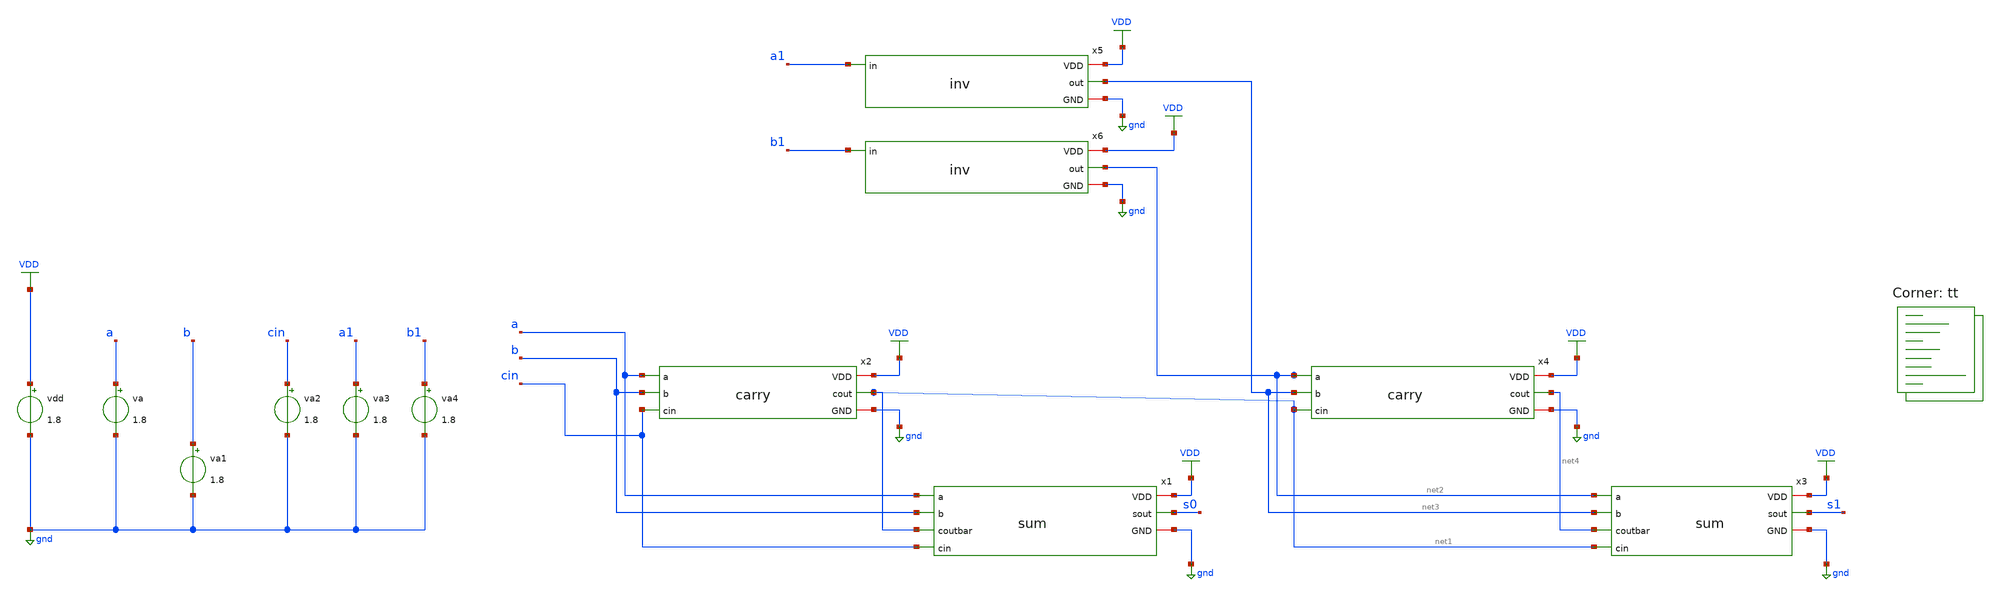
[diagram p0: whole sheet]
** sch_path: assignments/assignment7/assign1a.sch
**.subckt assign1a
x1 VDD a b net1 cin s0 gnd sum
x2 VDD a b cin net1 gnd carry
x3 VDD net2 net3 net4 net1 s1 gnd sum
x4 VDD net2 net3 net1 net4 gnd carry
vdd VDD gnd 1.8
va a gnd 1.8
va1 b gnd 1.8
va2 cin gnd 1.8
va3 a1 gnd 1.8
va4 b1 gnd 1.8
x5 VDD a1 net3 gnd inv
x6 VDD b1 net2 gnd inv
**** begin user architecture code


.control
alter @va[pulse] = [ 1.8 0 10p 5p 5p ]
alter @va1[pulse] = [ 1.8 0 10p 5p 5p ]
alter @va2[pulse] = [ 0 1.8 10p 5p 5p ]
alter @va3[pulse] = [ 1.8 0 10p 5p 5p ]
alter @va4[pulse] = [ 1.8 0 10p 5p 5p ]

tran 1p 400p
meas tran delay_cin_net1 TRIG v(cin) VAL=0.9 RISE=1 TARG v(net1) VAL=0.9 FALL=1
meas tran delay_cin_s0 TRIG v(cin) VAL=0.9 RISE=1 TARG v(s0) VAL=0.9 CROSS=1
plot v(a) v(b) v(cin) v(s0)
.endc


.lib $::SKYWATER_MODELS/sky130.lib.spice tt
**** end user architecture code
**.ends

* expanding   symbol:  sum.sym # of pins=7
** sym_path: assignments/assignment7/sum.sym
** sch_path: assignments/assignment7/sum.sch
.subckt sum VDD a b coutbar cin sout GND
*.opin sout
*.ipin a
*.iopin VDD
*.iopin GND
*.ipin b
*.ipin coutbar
*.ipin cin
XM1 sout coutbar net4 GND sky130_fd_pr__nfet_01v8 L=0.15 W=0.84 nf=1 ad='int((nf+1)/2) * W/nf * 0.29'
+ as='int((nf+2)/2) * W/nf * 0.29' pd='2*int((nf+1)/2) * (W/nf + 0.29)' ps='2*int((nf+2)/2) * (W/nf + 0.29)'
+ nrd='0.29 / W' nrs='0.29 / W' sa=0 sb=0 sd=0 mult=1 m=1
XM2 net1 b VDD VDD sky130_fd_pr__pfet_01v8 L=0.15 W=1.68 nf=1 ad='int((nf+1)/2) * W/nf * 0.29' as='int((nf+2)/2) * W/nf * 0.29'
+ pd='2*int((nf+1)/2) * (W/nf + 0.29)' ps='2*int((nf+2)/2) * (W/nf + 0.29)' nrd='0.29 / W' nrs='0.29 / W'
+ sa=0 sb=0 sd=0 mult=1 m=1
XM4 sout coutbar net1 VDD sky130_fd_pr__pfet_01v8 L=0.15 W=1.68 nf=1 ad='int((nf+1)/2) * W/nf * 0.29'
+ as='int((nf+2)/2) * W/nf * 0.29' pd='2*int((nf+1)/2) * (W/nf + 0.29)' ps='2*int((nf+2)/2) * (W/nf + 0.29)'
+ nrd='0.29 / W' nrs='0.29 / W' sa=0 sb=0 sd=0 mult=1 m=1
XM5 net1 a VDD VDD sky130_fd_pr__pfet_01v8 L=0.15 W=1.68 nf=1 ad='int((nf+1)/2) * W/nf * 0.29' as='int((nf+2)/2) * W/nf * 0.29'
+ pd='2*int((nf+1)/2) * (W/nf + 0.29)' ps='2*int((nf+2)/2) * (W/nf + 0.29)' nrd='0.29 / W' nrs='0.29 / W'
+ sa=0 sb=0 sd=0 mult=1 m=1
XM6 net1 cin VDD VDD sky130_fd_pr__pfet_01v8 L=0.15 W=1.68 nf=1 ad='int((nf+1)/2) * W/nf * 0.29' as='int((nf+2)/2) * W/nf * 0.29'
+ pd='2*int((nf+1)/2) * (W/nf + 0.29)' ps='2*int((nf+2)/2) * (W/nf + 0.29)' nrd='0.29 / W' nrs='0.29 / W'
+ sa=0 sb=0 sd=0 mult=1 m=1
XM7 net3 a VDD VDD sky130_fd_pr__pfet_01v8 L=0.15 W=1.68 nf=1 ad='int((nf+1)/2) * W/nf * 0.29' as='int((nf+2)/2) * W/nf * 0.29'
+ pd='2*int((nf+1)/2) * (W/nf + 0.29)' ps='2*int((nf+2)/2) * (W/nf + 0.29)' nrd='0.29 / W' nrs='0.29 / W'
+ sa=0 sb=0 sd=0 mult=1 m=1
XM3 net2 b net3 VDD sky130_fd_pr__pfet_01v8 L=0.15 W=1.68 nf=1 ad='int((nf+1)/2) * W/nf * 0.29' as='int((nf+2)/2) * W/nf * 0.29'
+ pd='2*int((nf+1)/2) * (W/nf + 0.29)' ps='2*int((nf+2)/2) * (W/nf + 0.29)' nrd='0.29 / W' nrs='0.29 / W'
+ sa=0 sb=0 sd=0 mult=1 m=1
XM8 sout cin net2 VDD sky130_fd_pr__pfet_01v8 L=0.15 W=1.68 nf=1 ad='int((nf+1)/2) * W/nf * 0.29' as='int((nf+2)/2) * W/nf * 0.29'
+ pd='2*int((nf+1)/2) * (W/nf + 0.29)' ps='2*int((nf+2)/2) * (W/nf + 0.29)' nrd='0.29 / W' nrs='0.29 / W'
+ sa=0 sb=0 sd=0 mult=1 m=1
XM9 net4 a GND GND sky130_fd_pr__nfet_01v8 L=0.15 W=0.84 nf=1 ad='int((nf+1)/2) * W/nf * 0.29' as='int((nf+2)/2) * W/nf * 0.29'
+ pd='2*int((nf+1)/2) * (W/nf + 0.29)' ps='2*int((nf+2)/2) * (W/nf + 0.29)' nrd='0.29 / W' nrs='0.29 / W'
+ sa=0 sb=0 sd=0 mult=1 m=1
XM10 net4 b GND GND sky130_fd_pr__nfet_01v8 L=0.15 W=0.84 nf=1 ad='int((nf+1)/2) * W/nf * 0.29' as='int((nf+2)/2) * W/nf * 0.29'
+ pd='2*int((nf+1)/2) * (W/nf + 0.29)' ps='2*int((nf+2)/2) * (W/nf + 0.29)' nrd='0.29 / W' nrs='0.29 / W'
+ sa=0 sb=0 sd=0 mult=1 m=1
XM11 net4 cin GND GND sky130_fd_pr__nfet_01v8 L=0.15 W=0.84 nf=1 ad='int((nf+1)/2) * W/nf * 0.29' as='int((nf+2)/2) * W/nf * 0.29'
+ pd='2*int((nf+1)/2) * (W/nf + 0.29)' ps='2*int((nf+2)/2) * (W/nf + 0.29)' nrd='0.29 / W' nrs='0.29 / W'
+ sa=0 sb=0 sd=0 mult=1 m=1
XM12 sout cin net6 GND sky130_fd_pr__nfet_01v8 L=0.15 W=0.84 nf=1 ad='int((nf+1)/2) * W/nf * 0.29' as='int((nf+2)/2) * W/nf * 0.29'
+ pd='2*int((nf+1)/2) * (W/nf + 0.29)' ps='2*int((nf+2)/2) * (W/nf + 0.29)' nrd='0.29 / W' nrs='0.29 / W'
+ sa=0 sb=0 sd=0 mult=1 m=1
XM13 net6 b net5 GND sky130_fd_pr__nfet_01v8 L=0.15 W=0.84 nf=1 ad='int((nf+1)/2) * W/nf * 0.29' as='int((nf+2)/2) * W/nf * 0.29'
+ pd='2*int((nf+1)/2) * (W/nf + 0.29)' ps='2*int((nf+2)/2) * (W/nf + 0.29)' nrd='0.29 / W' nrs='0.29 / W'
+ sa=0 sb=0 sd=0 mult=1 m=1
XM14 net5 a GND GND sky130_fd_pr__nfet_01v8 L=0.15 W=0.84 nf=1 ad='int((nf+1)/2) * W/nf * 0.29' as='int((nf+2)/2) * W/nf * 0.29'
+ pd='2*int((nf+1)/2) * (W/nf + 0.29)' ps='2*int((nf+2)/2) * (W/nf + 0.29)' nrd='0.29 / W' nrs='0.29 / W'
+ sa=0 sb=0 sd=0 mult=1 m=1
.ends


* expanding   symbol:  carry.sym # of pins=6
** sym_path: assignments/assignment7/carry.sym
** sch_path: assignments/assignment7/carry.sch
.subckt carry VDD a b cin cout GND
*.opin cout
*.ipin a
*.iopin VDD
*.iopin GND
*.ipin b
*.ipin cin
XM1 cout cin net3 GND sky130_fd_pr__nfet_01v8 L=0.15 W=0.84 nf=2 ad='int((nf+1)/2) * W/nf * 0.29' as='int((nf+2)/2) * W/nf * 0.29'
+ pd='2*int((nf+1)/2) * (W/nf + 0.29)' ps='2*int((nf+2)/2) * (W/nf + 0.29)' nrd='0.29 / W' nrs='0.29 / W'
+ sa=0 sb=0 sd=0 mult=1 m=1
XM2 net1 b VDD VDD sky130_fd_pr__pfet_01v8 L=0.15 W=1.68 nf=4 ad='int((nf+1)/2) * W/nf * 0.29' as='int((nf+2)/2) * W/nf * 0.29'
+ pd='2*int((nf+1)/2) * (W/nf + 0.29)' ps='2*int((nf+2)/2) * (W/nf + 0.29)' nrd='0.29 / W' nrs='0.29 / W'
+ sa=0 sb=0 sd=0 mult=1 m=1
XM3 net3 a GND GND sky130_fd_pr__nfet_01v8 L=0.15 W=0.84 nf=2 ad='int((nf+1)/2) * W/nf * 0.29' as='int((nf+2)/2) * W/nf * 0.29'
+ pd='2*int((nf+1)/2) * (W/nf + 0.29)' ps='2*int((nf+2)/2) * (W/nf + 0.29)' nrd='0.29 / W' nrs='0.29 / W'
+ sa=0 sb=0 sd=0 mult=1 m=1
XM4 cout cin net1 VDD sky130_fd_pr__pfet_01v8 L=0.15 W=1.68 nf=4 ad='int((nf+1)/2) * W/nf * 0.29' as='int((nf+2)/2) * W/nf * 0.29'
+ pd='2*int((nf+1)/2) * (W/nf + 0.29)' ps='2*int((nf+2)/2) * (W/nf + 0.29)' nrd='0.29 / W' nrs='0.29 / W'
+ sa=0 sb=0 sd=0 mult=1 m=1
XM5 net1 a VDD VDD sky130_fd_pr__pfet_01v8 L=0.15 W=1.68 nf=4 ad='int((nf+1)/2) * W/nf * 0.29' as='int((nf+2)/2) * W/nf * 0.29'
+ pd='2*int((nf+1)/2) * (W/nf + 0.29)' ps='2*int((nf+2)/2) * (W/nf + 0.29)' nrd='0.29 / W' nrs='0.29 / W'
+ sa=0 sb=0 sd=0 mult=1 m=1
XM6 net2 a VDD VDD sky130_fd_pr__pfet_01v8 L=0.15 W=1.68 nf=4 ad='int((nf+1)/2) * W/nf * 0.29' as='int((nf+2)/2) * W/nf * 0.29'
+ pd='2*int((nf+1)/2) * (W/nf + 0.29)' ps='2*int((nf+2)/2) * (W/nf + 0.29)' nrd='0.29 / W' nrs='0.29 / W'
+ sa=0 sb=0 sd=0 mult=1 m=1
XM7 cout b net2 VDD sky130_fd_pr__pfet_01v8 L=0.15 W=1.68 nf=4 ad='int((nf+1)/2) * W/nf * 0.29' as='int((nf+2)/2) * W/nf * 0.29'
+ pd='2*int((nf+1)/2) * (W/nf + 0.29)' ps='2*int((nf+2)/2) * (W/nf + 0.29)' nrd='0.29 / W' nrs='0.29 / W'
+ sa=0 sb=0 sd=0 mult=1 m=1
XM8 net3 b GND GND sky130_fd_pr__nfet_01v8 L=0.15 W=0.84 nf=2 ad='int((nf+1)/2) * W/nf * 0.29' as='int((nf+2)/2) * W/nf * 0.29'
+ pd='2*int((nf+1)/2) * (W/nf + 0.29)' ps='2*int((nf+2)/2) * (W/nf + 0.29)' nrd='0.29 / W' nrs='0.29 / W'
+ sa=0 sb=0 sd=0 mult=1 m=1
XM9 cout a net4 GND sky130_fd_pr__nfet_01v8 L=0.15 W=0.84 nf=2 ad='int((nf+1)/2) * W/nf * 0.29' as='int((nf+2)/2) * W/nf * 0.29'
+ pd='2*int((nf+1)/2) * (W/nf + 0.29)' ps='2*int((nf+2)/2) * (W/nf + 0.29)' nrd='0.29 / W' nrs='0.29 / W'
+ sa=0 sb=0 sd=0 mult=1 m=1
XM10 net4 b GND GND sky130_fd_pr__nfet_01v8 L=0.15 W=0.84 nf=2 ad='int((nf+1)/2) * W/nf * 0.29' as='int((nf+2)/2) * W/nf * 0.29'
+ pd='2*int((nf+1)/2) * (W/nf + 0.29)' ps='2*int((nf+2)/2) * (W/nf + 0.29)' nrd='0.29 / W' nrs='0.29 / W'
+ sa=0 sb=0 sd=0 mult=1 m=1
.ends


* expanding   symbol:  inv.sym # of pins=4
** sym_path: assignments/assignment6/inv.sym
** sch_path: assignments/assignment6/inv.sch
.subckt inv VDD in out GND
*.ipin in
*.iopin GND
*.iopin VDD
*.opin out
XM3 out in GND GND sky130_fd_pr__nfet_01v8 L=0.15 W=0.42 nf=1 ad='int((nf+1)/2) * W/nf * 0.29' as='int((nf+2)/2) * W/nf * 0.29'
+ pd='2*int((nf+1)/2) * (W/nf + 0.29)' ps='2*int((nf+2)/2) * (W/nf + 0.29)' nrd='0.29 / W' nrs='0.29 / W'
+ sa=0 sb=0 sd=0 mult=1 m=1
XM4 out in VDD VDD sky130_fd_pr__pfet_01v8 L=0.15 W=0.84 nf=1 ad='int((nf+1)/2) * W/nf * 0.29' as='int((nf+2)/2) * W/nf * 0.29'
+ pd='2*int((nf+1)/2) * (W/nf + 0.29)' ps='2*int((nf+2)/2) * (W/nf + 0.29)' nrd='0.29 / W' nrs='0.29 / W'
+ sa=0 sb=0 sd=0 mult=1 m=1
.ends

.GLOBAL VDD
.GLOBAL gnd
.end
